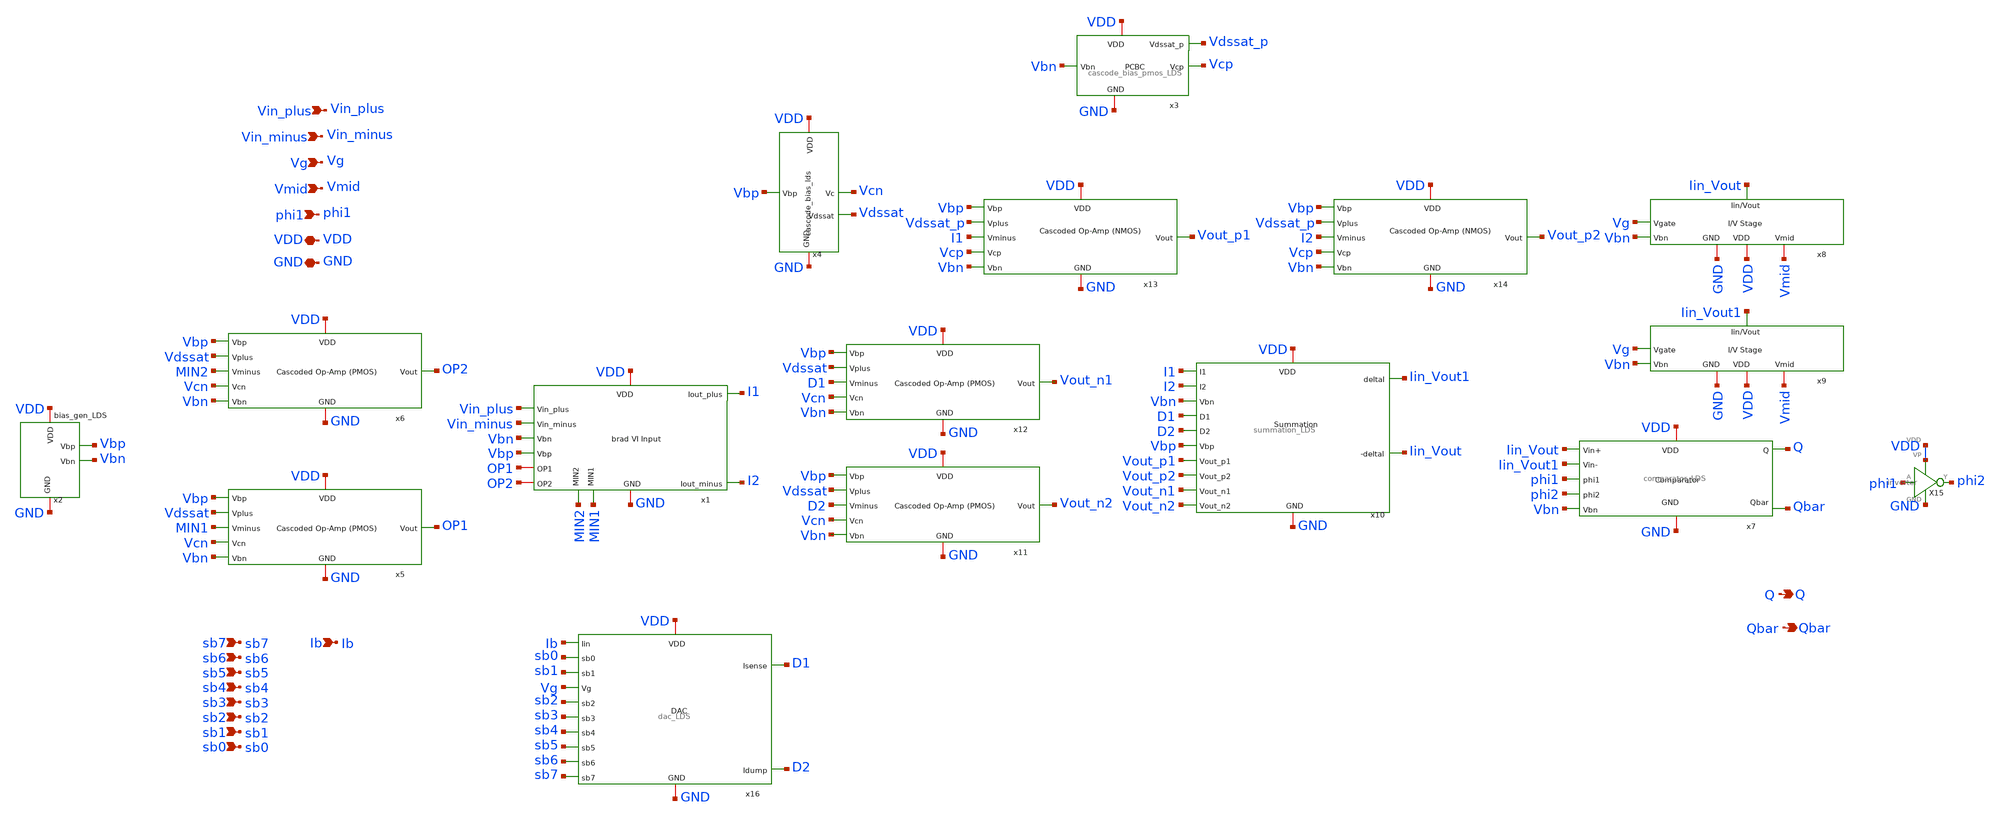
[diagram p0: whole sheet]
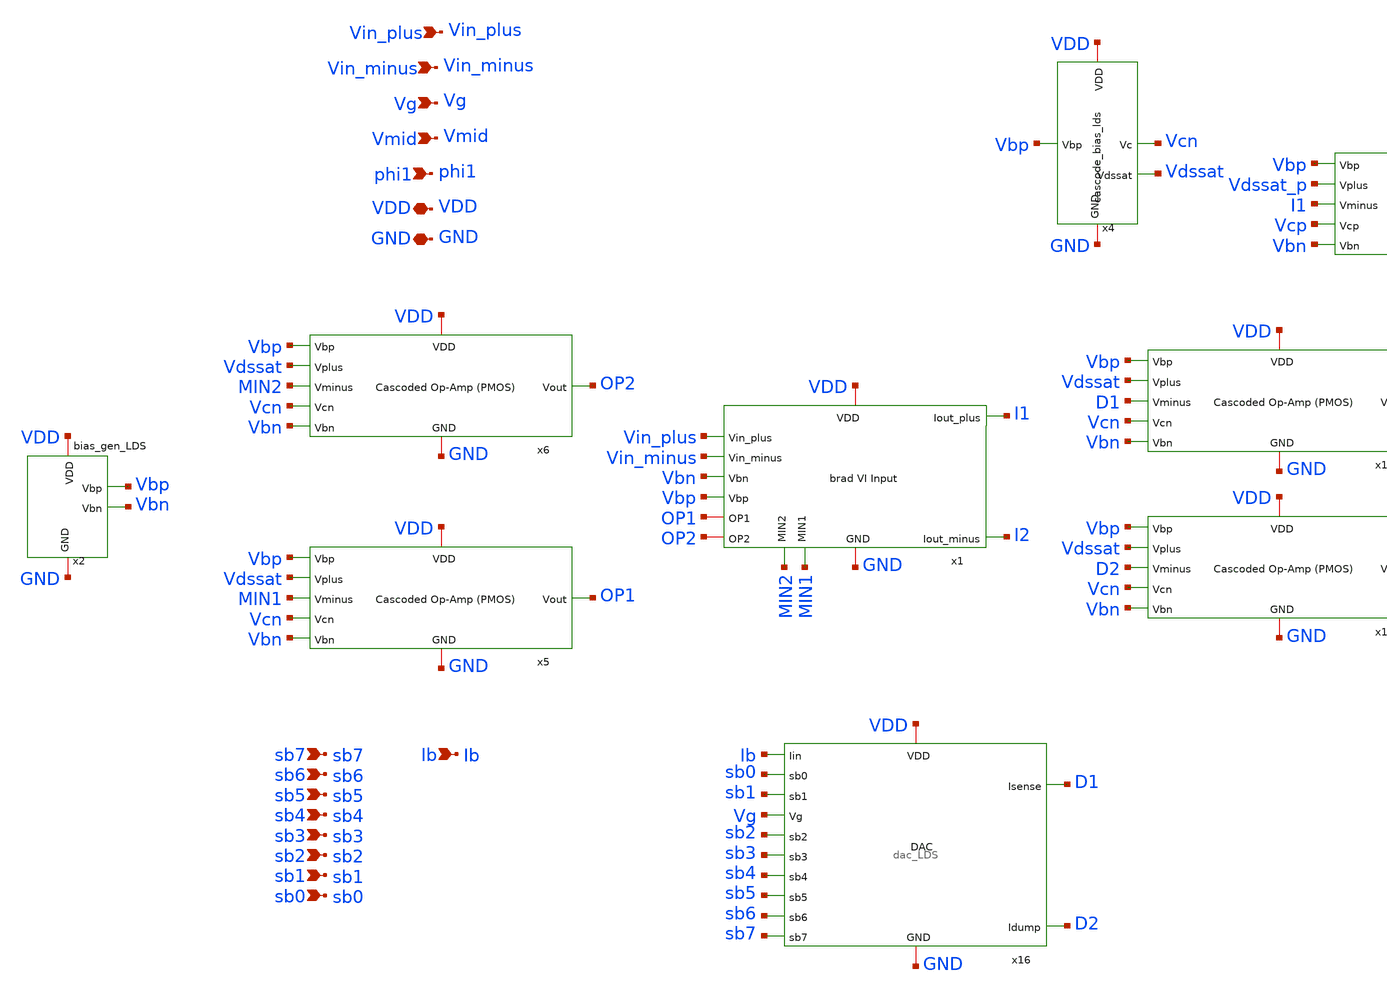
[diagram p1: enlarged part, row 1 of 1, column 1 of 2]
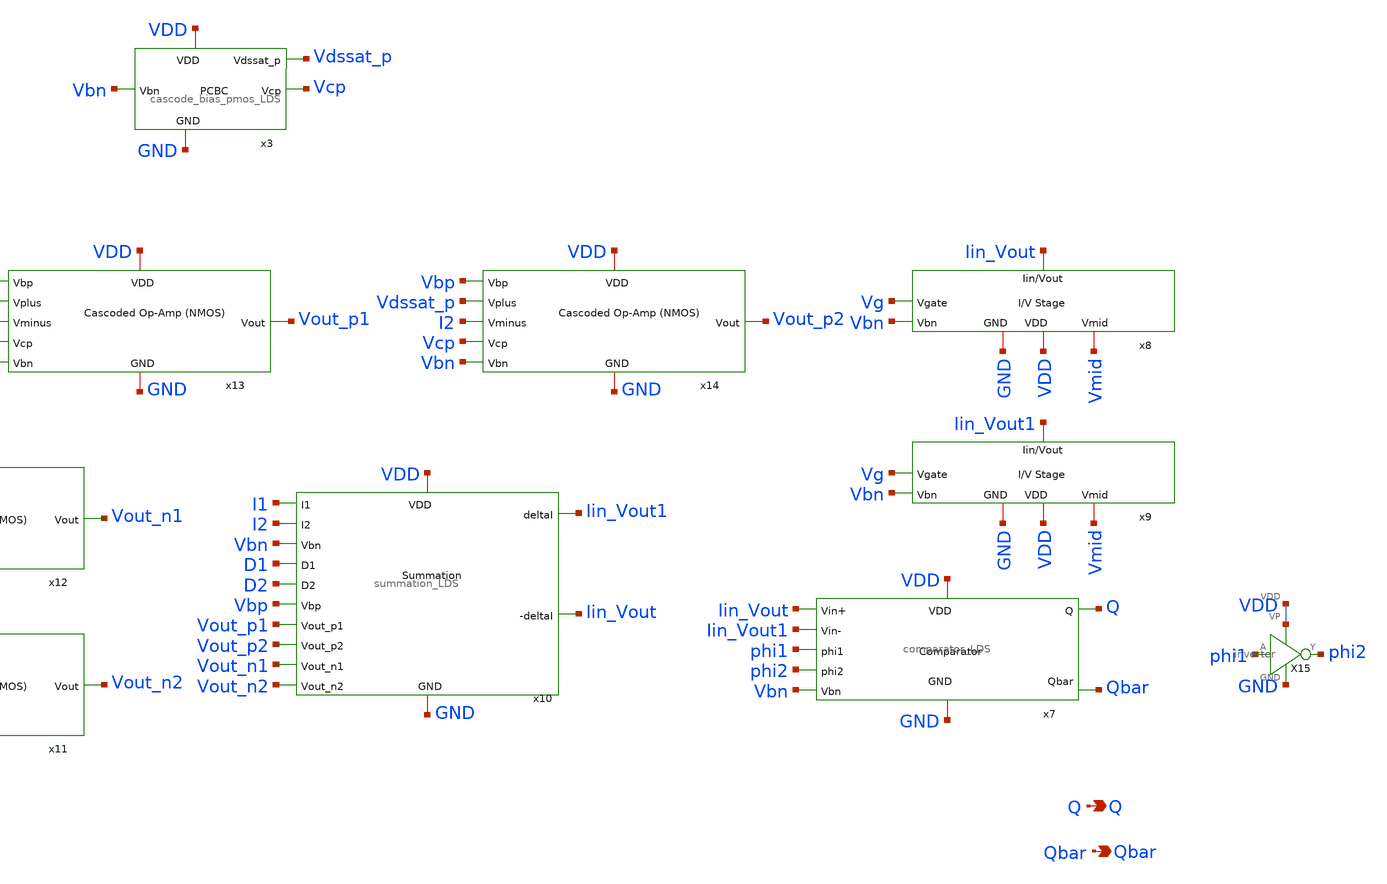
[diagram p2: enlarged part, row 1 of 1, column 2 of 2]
** sch_path: final/LDS/ADC_LDS.sch
**.subckt ADC_LDS Vin_plus Vin_minus Vg Vmid phi1 sb7 sb6 sb5 sb4 sb3 sb2 sb1 sb0 VDD GND Ib Q Qbar
*.ipin Vin_plus
*.ipin Vin_minus
*.ipin Vg
*.ipin Vmid
*.ipin phi1
*.ipin sb7
*.ipin sb6
*.ipin sb5
*.ipin sb4
*.ipin sb3
*.ipin sb2
*.ipin sb1
*.ipin sb0
*.iopin VDD
*.iopin GND
*.ipin Ib
*.opin Q
*.opin Qbar
x1 VDD I1 I2 Vin_plus Vin_minus Vbn Vbp GND OP1 OP2 MIN1 MIN2 brad_VI_input_LDS
x2 VDD Vbp GND Vbn bias_gen_LDS
x3 Vbn VDD GND Vcp Vdssat_p cascode_bias_pmos_LDS
x4 Vbp VDD Vcn GND Vdssat cascode_bias_lds
x5 Vbp Vdssat MIN1 Vcn Vbn VDD GND OP1 cascoded_opamp_pmos_LDS
x6 Vbp Vdssat MIN2 Vcn Vbn VDD GND OP2 cascoded_opamp_pmos_LDS
x7 VDD Vbn Iin_Vout Iin_Vout1 phi1 phi2 Q Qbar GND comparator_LDS
x8 Iin_Vout Vg Vmid Vbn GND VDD IV_converter_LDS
x9 Iin_Vout1 Vg Vmid Vbn GND VDD IV_converter_LDS
x10 VDD GND I1 I2 Vbn D1 D2 Iin_Vout1 Iin_Vout Vbp Vout_p1 Vout_p2 Vout_n1 Vout_n2 summation_LDS
x11 Vbp Vdssat D2 Vcn Vbn VDD GND Vout_n2 cascoded_opamp_pmos_LDS
x12 Vbp Vdssat D1 Vcn Vbn VDD GND Vout_n1 cascoded_opamp_pmos_LDS
x13 Vbp Vdssat_p I1 Vcp Vbn VDD GND Vout_p1 cascoded_opamp_LDS
x14 Vbp Vdssat_p I2 Vcp Vbn VDD GND Vout_p2 cascoded_opamp_LDS
X15 VDD phi1 phi2 GND VDD inverter
x16 sb0 VDD GND sb1 Vg sb2 sb3 D1 sb4 D2 sb5 sb6 sb7 Ib dac_LDS
**.ends
.end
